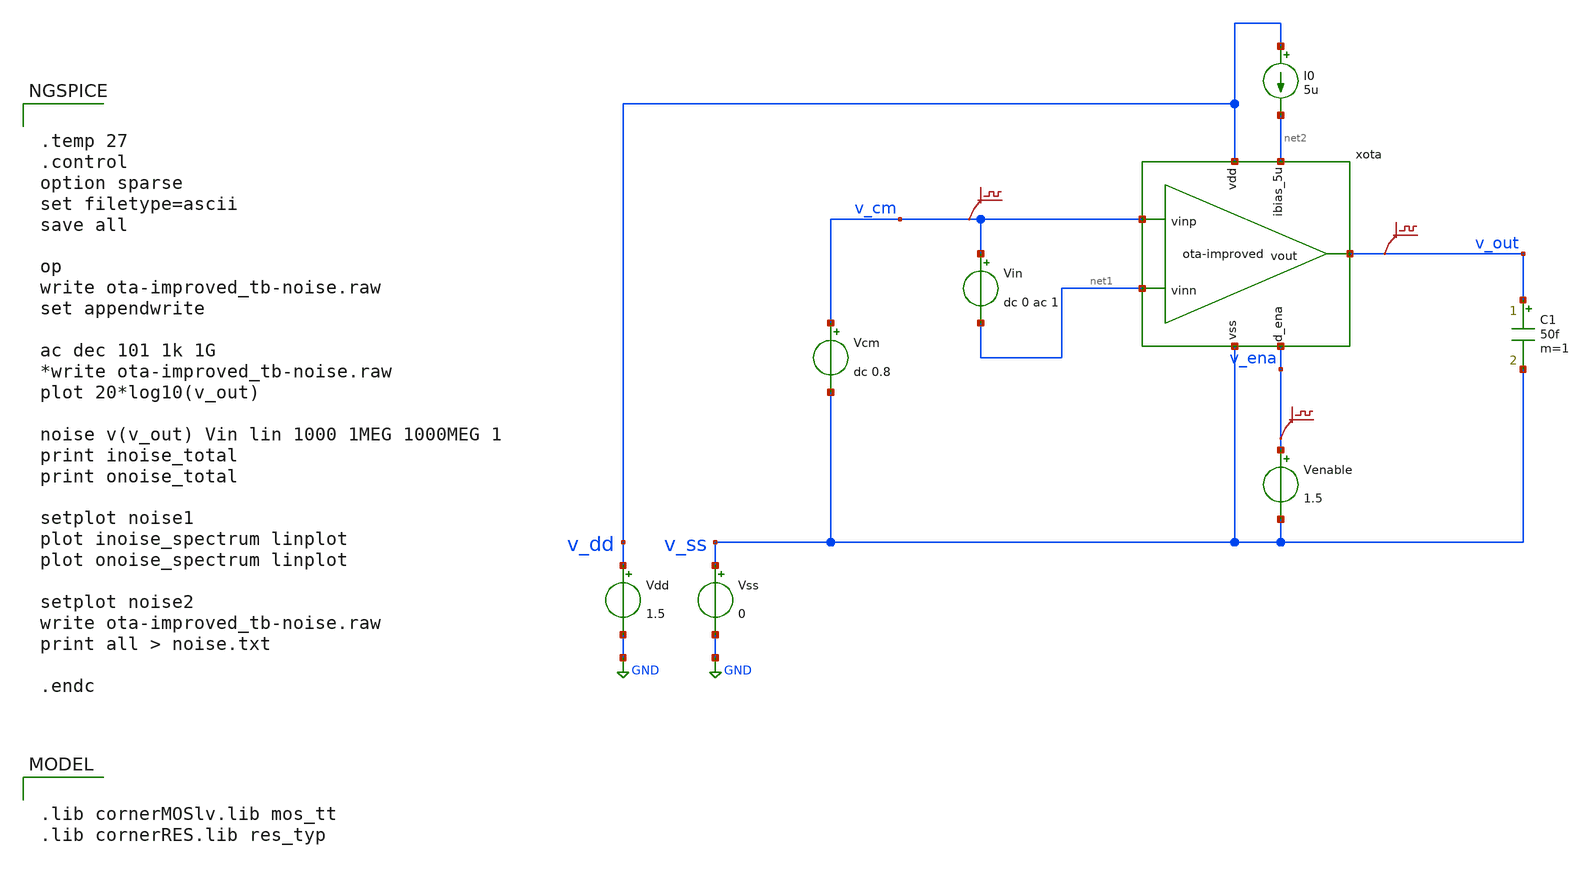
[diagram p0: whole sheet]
** sch_path: xschem/ota-improved_tb-noise.sch
* (c) 2024-2025 H. Pretl, Apache-2.0 license
**.subckt ota-improved_tb-noise
Vdd v_dd GND 1.5
xota v_dd v_out v_cm net1 net2 v_ena v_ss ota-improved
Vss v_ss GND 0
C1 v_out v_ss 50f m=1
Vcm v_cm v_ss dc 0.8
I0 v_dd net2 5u
Venable v_ena v_ss 1.5
.save v(v_cm)
.save v(v_out)
.save v(v_ena)
Vin v_cm net1 dc 0 ac 1
**** begin user architecture code

.lib cornerMOSlv.lib mos_tt
.lib cornerRES.lib res_typ



.temp 27
.control
option sparse
set filetype=ascii
save all

op
write ota-improved_tb-noise.raw
set appendwrite

ac dec 101 1k 1G
*write ota-improved_tb-noise.raw
plot 20*log10(v_out)

noise v(v_out) Vin lin 1000 1MEG 1000MEG 1
print inoise_total
print onoise_total

setplot noise1
plot inoise_spectrum linplot
plot onoise_spectrum linplot

setplot noise2
write ota-improved_tb-noise.raw
print all > noise.txt

.endc


**** end user architecture code
**.ends
.GLOBAL GND
.end
